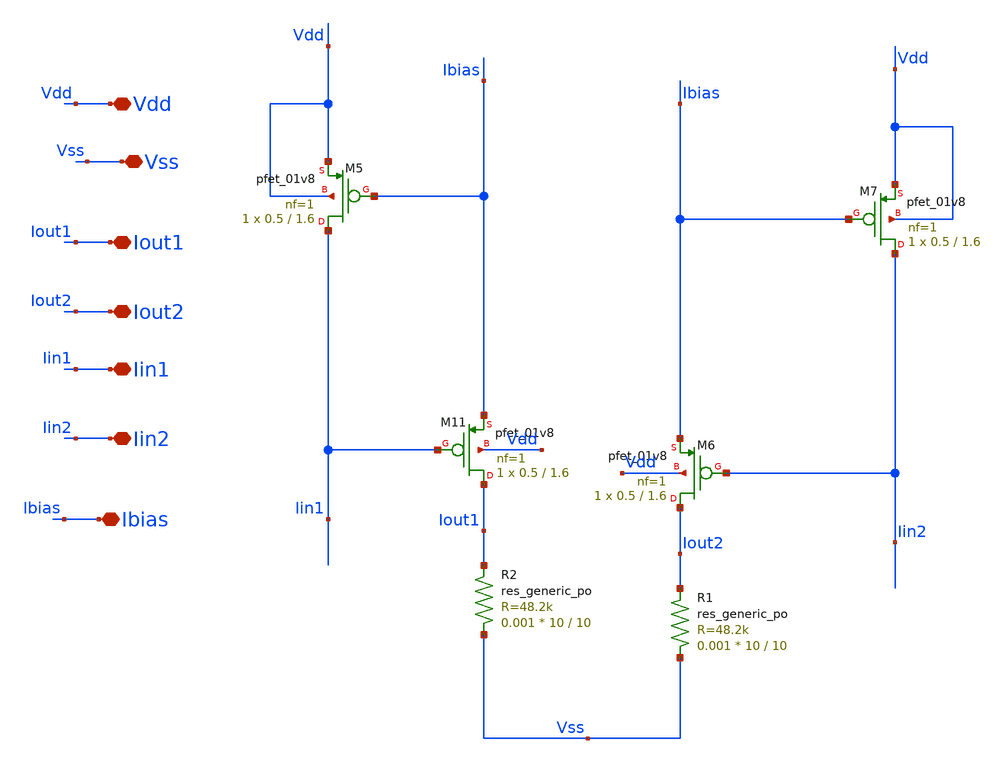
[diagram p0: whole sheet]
** sch_path: xschem/wta_pmos_tt.sch
**.subckt wta_pmos_tt Vdd Vss Iout1 Iout2 Iin1 Iin2 Ibias
*.iopin Vdd
*.iopin Vss
*.iopin Iout1
*.iopin Iout2
*.iopin Iin1
*.iopin Iin2
*.iopin Ibias
XM11 Iout1 Iin1 Ibias Vdd sky130_fd_pr__pfet_01v8 L=1.6 W=0.5 nf=1 ad='int((nf+1)/2) * W/nf * 0.29' as='int((nf+2)/2) * W/nf * 0.29'
+ pd='2*int((nf+1)/2) * (W/nf + 0.29)' ps='2*int((nf+2)/2) * (W/nf + 0.29)' nrd='0.29 / W' nrs='0.29 / W'
+ sa=0 sb=0 sd=0 mult=1 m=1
XM5 Iin1 Ibias Vdd Vdd sky130_fd_pr__pfet_01v8 L=1.6 W=0.5 nf=1 ad='int((nf+1)/2) * W/nf * 0.29' as='int((nf+2)/2) * W/nf * 0.29'
+ pd='2*int((nf+1)/2) * (W/nf + 0.29)' ps='2*int((nf+2)/2) * (W/nf + 0.29)' nrd='0.29 / W' nrs='0.29 / W'
+ sa=0 sb=0 sd=0 mult=1 m=1
XM6 Iout2 Iin2 Ibias Vdd sky130_fd_pr__pfet_01v8 L=1.6 W=0.5 nf=1 ad='int((nf+1)/2) * W/nf * 0.29' as='int((nf+2)/2) * W/nf * 0.29'
+ pd='2*int((nf+1)/2) * (W/nf + 0.29)' ps='2*int((nf+2)/2) * (W/nf + 0.29)' nrd='0.29 / W' nrs='0.29 / W'
+ sa=0 sb=0 sd=0 mult=1 m=1
XM7 Iin2 Ibias Vdd Vdd sky130_fd_pr__pfet_01v8 L=1.6 W=0.5 nf=1 ad='int((nf+1)/2) * W/nf * 0.29' as='int((nf+2)/2) * W/nf * 0.29'
+ pd='2*int((nf+1)/2) * (W/nf + 0.29)' ps='2*int((nf+2)/2) * (W/nf + 0.29)' nrd='0.29 / W' nrs='0.29 / W'
+ sa=0 sb=0 sd=0 mult=1 m=1
XR2 Vss Iout1 sky130_fd_pr__res_generic_po W=10 L=10 m=0.001
XR1 Vss Iout2 sky130_fd_pr__res_generic_po W=10 L=10 m=0.001
**.ends
.end
